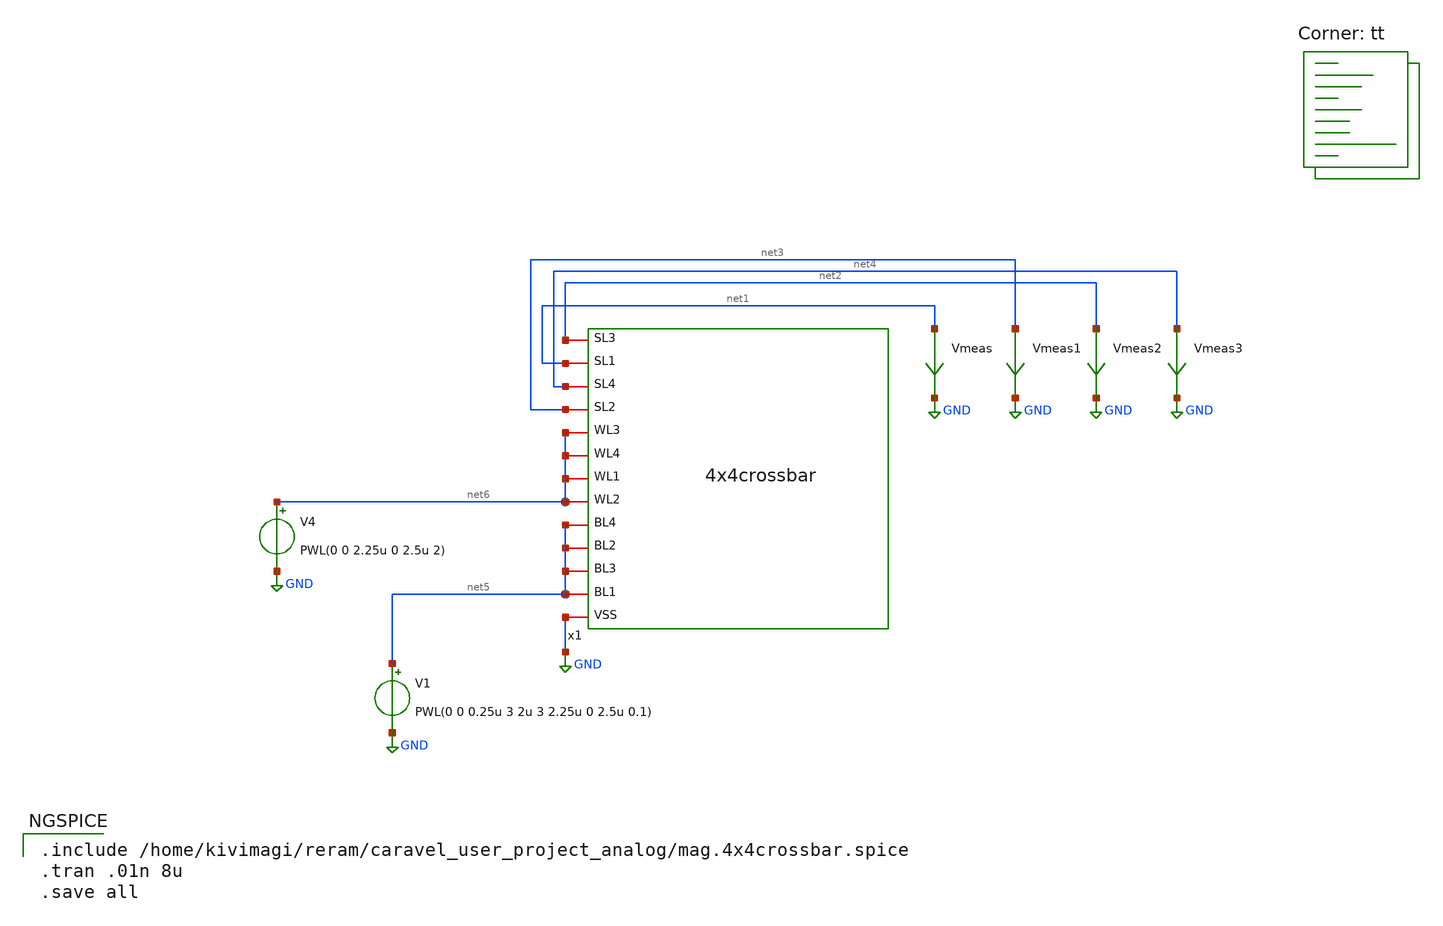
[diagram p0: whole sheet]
** sch_path: xschem/untitled.sch
**.subckt untitled
x1 GND net5 net5 net5 net5 net6 net6 net6 net6 net3 net4 net1 net2 4x4crossbar
Vmeas net1 GND 0
.save i(vmeas)
Vmeas1 net3 GND 0
.save i(vmeas1)
Vmeas2 net2 GND 0
.save i(vmeas2)
Vmeas3 net4 GND 0
.save i(vmeas3)
V4 net6 GND PWL(0 0 2.25u 0 2.5u 2)
V1 net5 GND PWL(0 0 0.25u 3 2u 3 2.25u 0 2.5u 0.1)
**** begin user architecture code
.lib $::SKYWATER_MODELS/sky130.lib.spice tt

.include /home/kivimagi/reram/caravel_user_project_analog/mag.4x4crossbar.spice
.tran .01n 8u
.save all


**** end user architecture code
**.ends
.GLOBAL GND
.end
